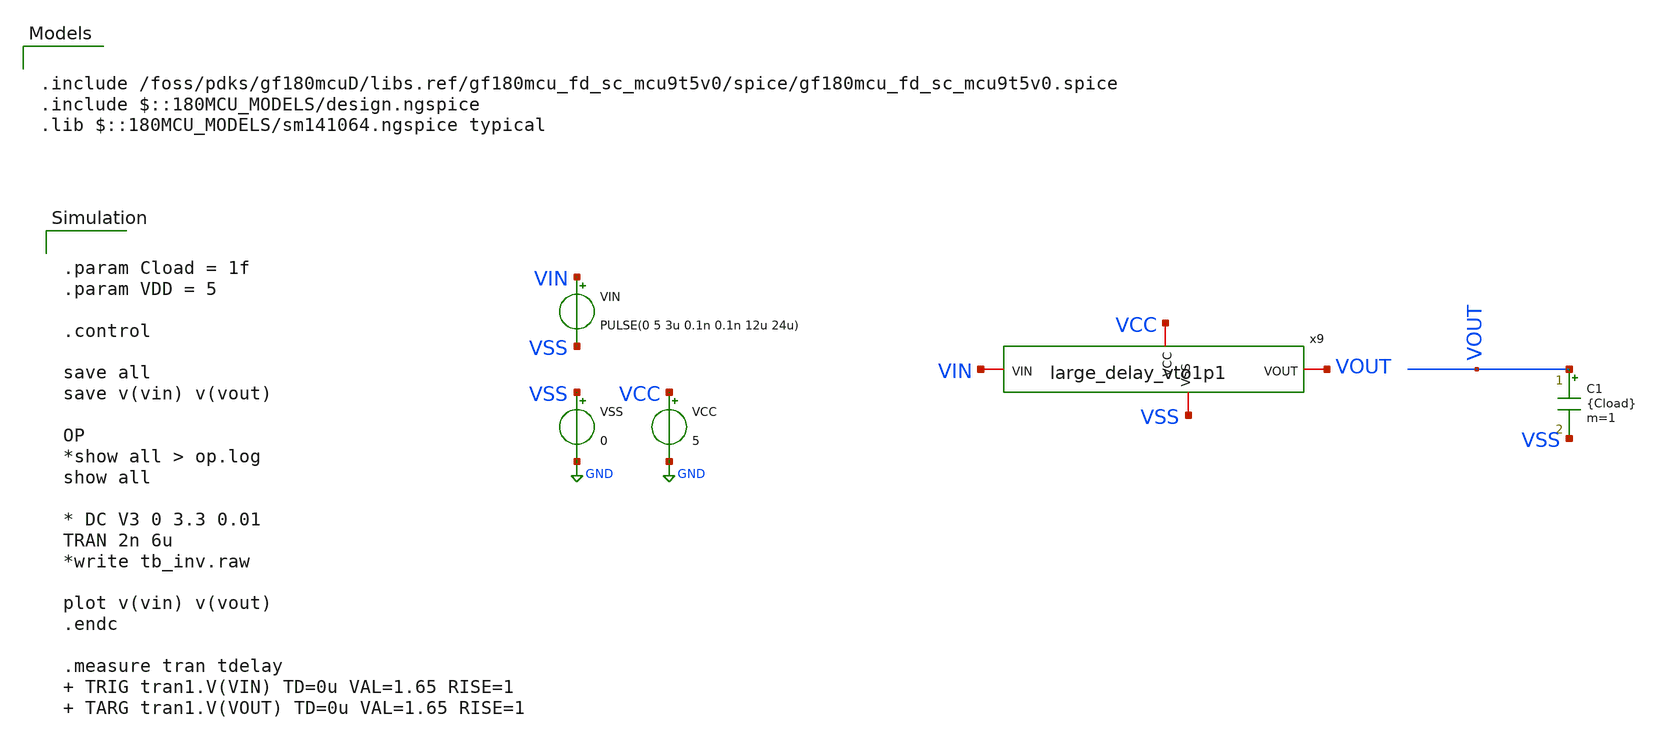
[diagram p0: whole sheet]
** sch_path: xschem/large_delay/tb_large_delay_vto1p1.sch
**.subckt tb_large_delay_vto1p1
VCC VCC GND 5
VSS VSS GND 0
VIN VIN VSS PULSE(0 5 3u 0.1n 0.1n 12u 24u)
C1 VOUT VSS {Cload} m=1
x9 VCC VSS VIN VOUT large_delay_vto1p1
**** begin user architecture code


.param Cload = 1f
.param VDD = 5

.control

save all
save v(vin) v(vout)

OP
*show all > op.log
show all

* DC V3 0 3.3 0.01
TRAN 2n 6u
*write tb_inv.raw

plot v(vin) v(vout)
.endc

.measure tran tdelay  TRIG tran1.V(VIN) TD=0u VAL=1.65 RISE=1  TARG tran1.V(VOUT) TD=0u VAL=1.65
+ RISE=1



.include /foss/pdks/gf180mcuD/libs.ref/gf180mcu_fd_sc_mcu9t5v0/spice/gf180mcu_fd_sc_mcu9t5v0.spice
.include $::180MCU_MODELS/design.ngspice
.lib $::180MCU_MODELS/sm141064.ngspice typical

**** end user architecture code
**.ends

* expanding   symbol:  large_delay_vto1p1.sym # of pins=4
** sym_path: xschem/gf180_digital/large_delay/large_delay_vto1p1.sym
** sch_path: xschem/gf180_digital/large_delay/large_delay_vto1p1.sch
.subckt large_delay_vto1p1 VDDd VSSd VIN VOUT
*.iopin VIN
*.iopin VOUT
*.iopin VDDd
*.iopin VSSd
x1 VIN VOUT VDDd VDDd VSSd VSSd gf180mcu_fd_sc_mcu9t5v0__dlya_1
.ends

.GLOBAL GND
.end
